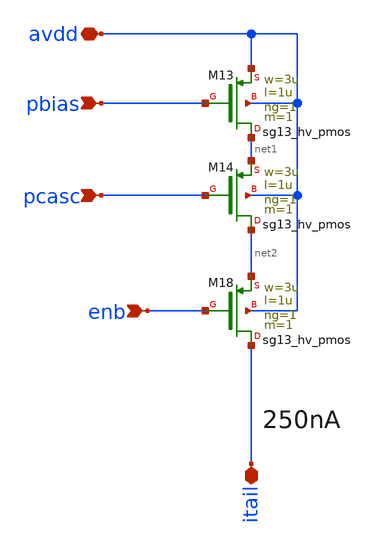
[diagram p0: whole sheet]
** sch_path: xschem/bias_pstack.sch
**.subckt bias_pstack avdd itail enb pcasc pbias
*.iopin avdd
*.iopin itail
*.ipin enb
*.ipin pcasc
*.ipin pbias
XM13 net1 pbias avdd avdd sg13_hv_pmos w=3u l=1u ng=1 m=1 mm_ok=1
XM18 itail enb net2 avdd sg13_hv_pmos w=3u l=1u ng=1 m=1 mm_ok=1
XM14 net2 pcasc net1 avdd sg13_hv_pmos w=3u l=1u ng=1 m=1 mm_ok=1
**.ends
.end
